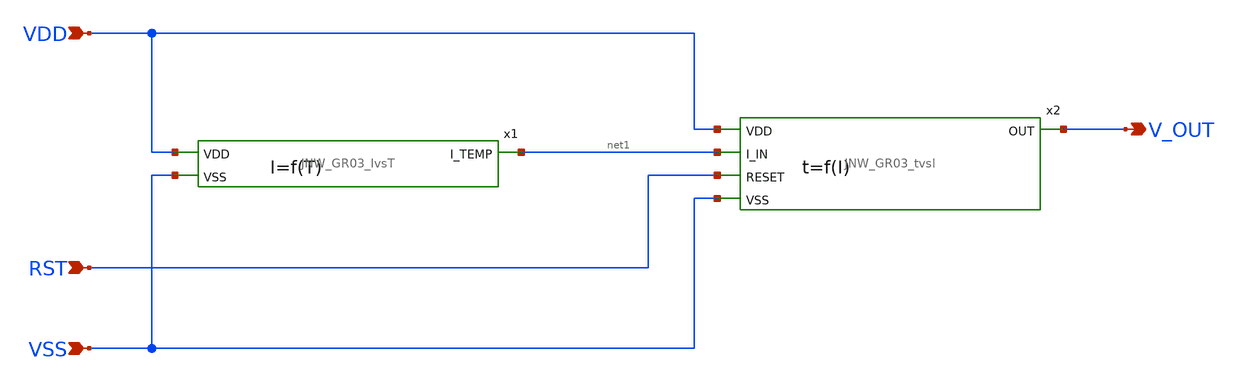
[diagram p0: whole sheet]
** sch_path: design/JNW_GR03_SKY130A/JNW_GR03_General.sch
**.subckt JNW_GR03_General VDD VSS V_OUT RST
*.ipin VDD
*.ipin VSS
*.opin V_OUT
*.ipin RST
x1 VDD net1 VSS JNW_GR03_IvsT
x2 VDD net1 V_OUT RST VSS JNW_GR03_tvsI
**.ends
.end
